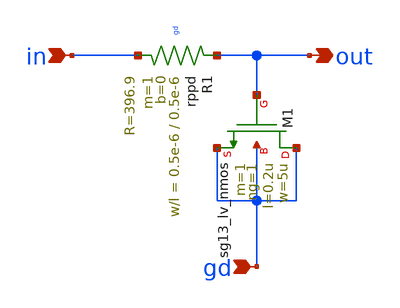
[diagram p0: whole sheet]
** sch_path: schematics/misc/RC_filter.sch
**.subckt RC_filter in out gd
*.ipin in
*.opin out
*.ipin gd
XR1 out in gd rppd w=0.5e-6 l=0.5e-6 m=1 b=0 mm_ok=1
XM1 gd out gd gd sg13_lv_nmos w=5u l=0.2u ng=1 m=1 mm_ok=1
**.ends
.end
